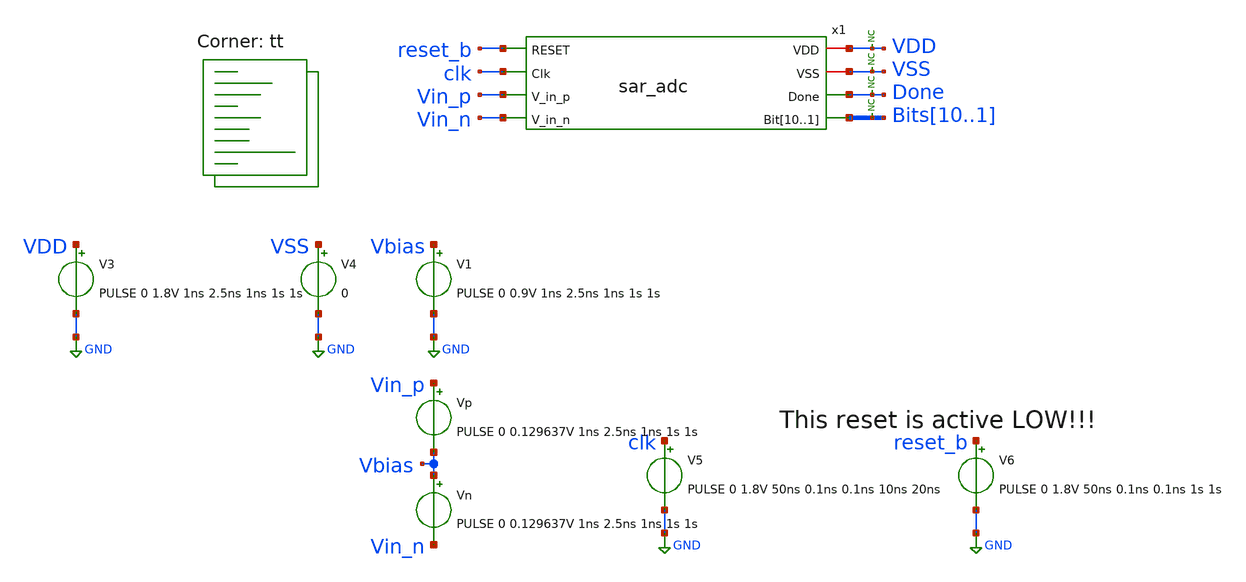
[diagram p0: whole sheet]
** sch_path: xschem/tests/sar_adc/sar_adc_max_sample_rate_test.sch
**.subckt sar_adc_max_sample_rate_test
V3 VDD GND PULSE 0 1.8V 1ns 2.5ns 1ns 1s 1s
V4 VSS GND 0
x1 VDD VSS reset_b clk Vin_p Vin_n Done Bits10 Bits9 Bits8 Bits7 Bits6 Bits5 Bits4 Bits3 Bits2 Bits1
+ sar_adc
Vn Vbias Vin_n PULSE 0 0.129637V 1ns 2.5ns 1ns 1s 1s
V5 clk GND PULSE 0 1.8V 50ns 0.1ns 0.1ns 10ns 20ns
V6 reset_b GND PULSE 0 1.8V 50ns 0.1ns 0.1ns 1s 1s
V1 Vbias GND PULSE 0 0.9V 1ns 2.5ns 1ns 1s 1s
Vp Vin_p Vbias PULSE 0 0.129637V 1ns 2.5ns 1ns 1s 1s
* noconn VDD
* noconn VSS
* noconn Done
* noconn Bits[10..1]
**** begin user architecture code

*.lib $::SKYWATER_MODELS/sky130.lib.spice tt

* .lib $::SKYWATER_MODELS/sky130.lib.spice.tt.red tt

.include $::SKYWATER_STDCELLS/sky130_fd_sc_hd.spice

.lib $::SKYWATER_MODELS/sky130.lib.spice tt



* ngspice commands
.options list acct opts
.control
save all
tran 0.5n 700ns uic

write sar_adc_max_sample_rate_test.raw

plot x1.x2.clk x1.x2.clk_n+2 x1.x2.clk_latch_n+4
plot x1.x2.pre_amp_n x1.x2.pre_amp_p
plot x1.sw_n_sp1 x1.sw_n_sp2+2 x1.sw_n_sp3+4 x1.sw_n_sp4+6 x1.sw_n_sp5+8 x1.sw_n_sp6+10
+ x1.sw_n_sp7+12 x1.sw_n_sp8+14 x1.sw_n_sp9+16
plot x1.sw_p_sp1 x1.sw_p_sp2+2 x1.sw_p_sp3+4 x1.sw_p_sp4+6 x1.sw_p_sp5+8 x1.sw_p_sp6+10
+ x1.sw_p_sp7+12 x1.sw_p_sp8+14 x1.sw_p_sp9+16
plot x1.sw_n1 x1.sw_n2+2 x1.sw_n3+4 x1.sw_n4+6 x1.sw_n5+8 x1.sw_n6+10 x1.sw_n7+12 x1.sw_n8+14
plot x1.sw_p1 x1.sw_p2+2 x1.sw_p3+4 x1.sw_p4+6 x1.sw_p5+8 x1.sw_p6+10 x1.sw_p7+12 x1.sw_p8+14
plot Done-4 Vin_p-Vin_n-2 bits1 bits2+2 bits3+4 bits4+6 bits5+8 bits6+10 bits7+12 bits8+14 bits9+16
+ bits10+18
plot x1.vsampled_p x1.vsampled_n x1.vsampled_p-x1.vsampled_n x1.sw_sample-2 x1.comp_out_p+2
+ x1.comp_out_n-2
plot x1.vcomp_q x1.comp_out_p x1.x5.net24
plot x1.x1.cycle0 x1.x1.cycle1 x1.x1.cycle2 x1.x1.cycle3 x1.x1.cycle4 x1.x1.cycle5 x1.x1.cycle6
+ x1.x1.cycle7 x1.x1.cycle8 x1.x1.cycle9 x1.x1.cycle10 x1.x1.cycle11 x1.x1.cycle12 x1.x1.cycle13 x1.x1.cycle14
+ x1.x1.cycle15 x1.controller_clk+2
* write sar_adc_test.raw
* * Go to the const plot
* setplot const
*
* let vdiff = -0.34V
* let vmax = 0.34V
* let vdelta = 0.04;
* let runs = 0
*
* * Insert vector names and set only one scale
* set wr_vecnames
* set wr_singlescale
*
* * set the hcopy type
* set hcopydevtype=svg
*
* let total_runs = ceil(($&vmax - $&vdiff) / $&vdelta)
* let out_bits = vector($&total_runs*10)
* reshape out_bits[10][$&total_runs]
* let in_diff_v= vector($&total_runs)
* let vsampled_p = vector($&total_runs)
* let vsampled_n = vector($&total_runs)
*
* while vdiff le $&vmax
* 	* Alter the voltages
* 	alter \@Vp[pulse] = [ 0 $&vdiff 1n 1u 1n 1 1 ] $ vector
* 	alter \@Vn[pulse] = [ 0 $&vdiff 1n 1u 1n 1 1 ] $ vector
*
* 	* Run the tran
* 	* tran creates a new plot starting with tran1
* 	tran 0.1n 240n uic
*
* 	set pltfile1 = plot_converg_{$&runs}_{$&vdiff}.svg
* 	set pltfile2 = plot_input_v_{$&runs}_{$&vdiff}.svg
* 	set pltfile3 = plot_clks_{$&runs}_{$&vdiff}.svg
* 	set plttitle = run{$&runs}_vin{$&vdiff}
* 	hardcopy $pltfile1 x1.vsampled_p x1.vsampled_n x1.vsampled_p-x1.vsampled_n x1.sw_sample-2
*+ x1.comp_out_p+2 x1.comp_out_n-2 title $plttitle
* 	*hardcopy $pltfile2 vin_p vin_n vss vdd vbias title $plttitle
* 	hardcopy $pltfile3 x1.x1.cycle0 x1.x1.cycle1 x1.x1.cycle2 x1.x1.cycle3 x1.x1.cycle4 x1.x1.cycle5
*+ x1.x1.cycle6 x1.x1.cycle7 x1.x1.cycle8 x1.x1.cycle9 x1.x1.cycle10 x1.x1.cycle11 x1.x1.cycle12 x1.x1.cycle13
*+ x1.x1.cycle14 x1.x1.cycle15 x1.controller_clk+2 title $plttitle
*
*
*
* 	* Measure the max to find the output
* 	meas tran max_bit0 MAX v(bits1) from=200n to=205n
* 	meas tran max_bit1 MAX v(bits2) from=200n to=205n
* 	meas tran max_bit2 MAX v(bits3) from=200n to=205n
* 	meas tran max_bit3 MAX v(bits4) from=200n to=205n
* 	meas tran max_bit4 MAX v(bits5) from=200n to=205n
* 	meas tran max_bit5 MAX v(bits6) from=200n to=205n
* 	meas tran max_bit6 MAX v(bits7) from=200n to=205n
* 	meas tran max_bit7 MAX v(bits8) from=200n to=205n
* 	meas tran max_bit8 MAX v(bits9) from=200n to=205n
* 	meas tran max_bit9 MAX v(bits10) from=200n to=205n
* 	meas tran avg_vsampled_p AVG v(x1.vsampled_p) from=190n to=195n
* 	meas tran avg_vsampled_n AVG v(x1.vsampled_n) from=190n to=195n
*
*
* 	* Create variables
* 	set max_bit0 = $&max_bit0
* 	set max_bit1 = $&max_bit1
* 	set max_bit2 = $&max_bit2
* 	set max_bit3 = $&max_bit3
* 	set max_bit4 = $&max_bit4
* 	set max_bit5 = $&max_bit5
* 	set max_bit6 = $&max_bit6
* 	set max_bit7 = $&max_bit7
* 	set max_bit8 = $&max_bit8
* 	set max_bit9 = $&max_bit9
* 	set vdiff = $&vdiff
* 	set vsampled_p = $&avg_vsampled_p
* 	set vsampled_n = $&avg_vsampled_n
*
* 	* Switch to constants plot
* 	setplot const
* 	*compose out_bits values $&out_bits $p_max $n_max
* 	let in_diff_v[$&runs] = $vdiff
* 	let vsampled_p[$&runs] = $vsampled_p
* 	let vsampled_n[$&runs] = $vsampled_n
* 	let out_bits[0][$&runs] = $max_bit0
* 	let out_bits[1][$&runs] = $max_bit1
* 	let out_bits[2][$&runs] = $max_bit2
* 	let out_bits[3][$&runs] = $max_bit3
* 	let out_bits[4][$&runs] = $max_bit4
* 	let out_bits[5][$&runs] = $max_bit5
* 	let out_bits[6][$&runs] = $max_bit6
* 	let out_bits[7][$&runs] = $max_bit7
* 	let out_bits[8][$&runs] = $max_bit8
* 	let out_bits[9][$&runs] = $max_bit9
*
* 	* set the iterators
* 	echo run $&runs
* 	let vdiff = vdiff + vdelta
* 	let runs = runs + 1
*
* 	* Destroy the transient plot to release memory
* 	destroy tran1
*
* end
*
* * switch to the const plot
* setplot const
* compose def_scale start=1 stop=$&total_runs step=1
* setscale def_scale
* echo Writing out_bits.txt
* wrdata out_bits.txt vsampled_p vsampled_n in_diff_v out_bits
*
* echo
* echo Total Runs = $&runs
* echo
.endc



**** end user architecture code
**.ends
.GLOBAL GND
.end
